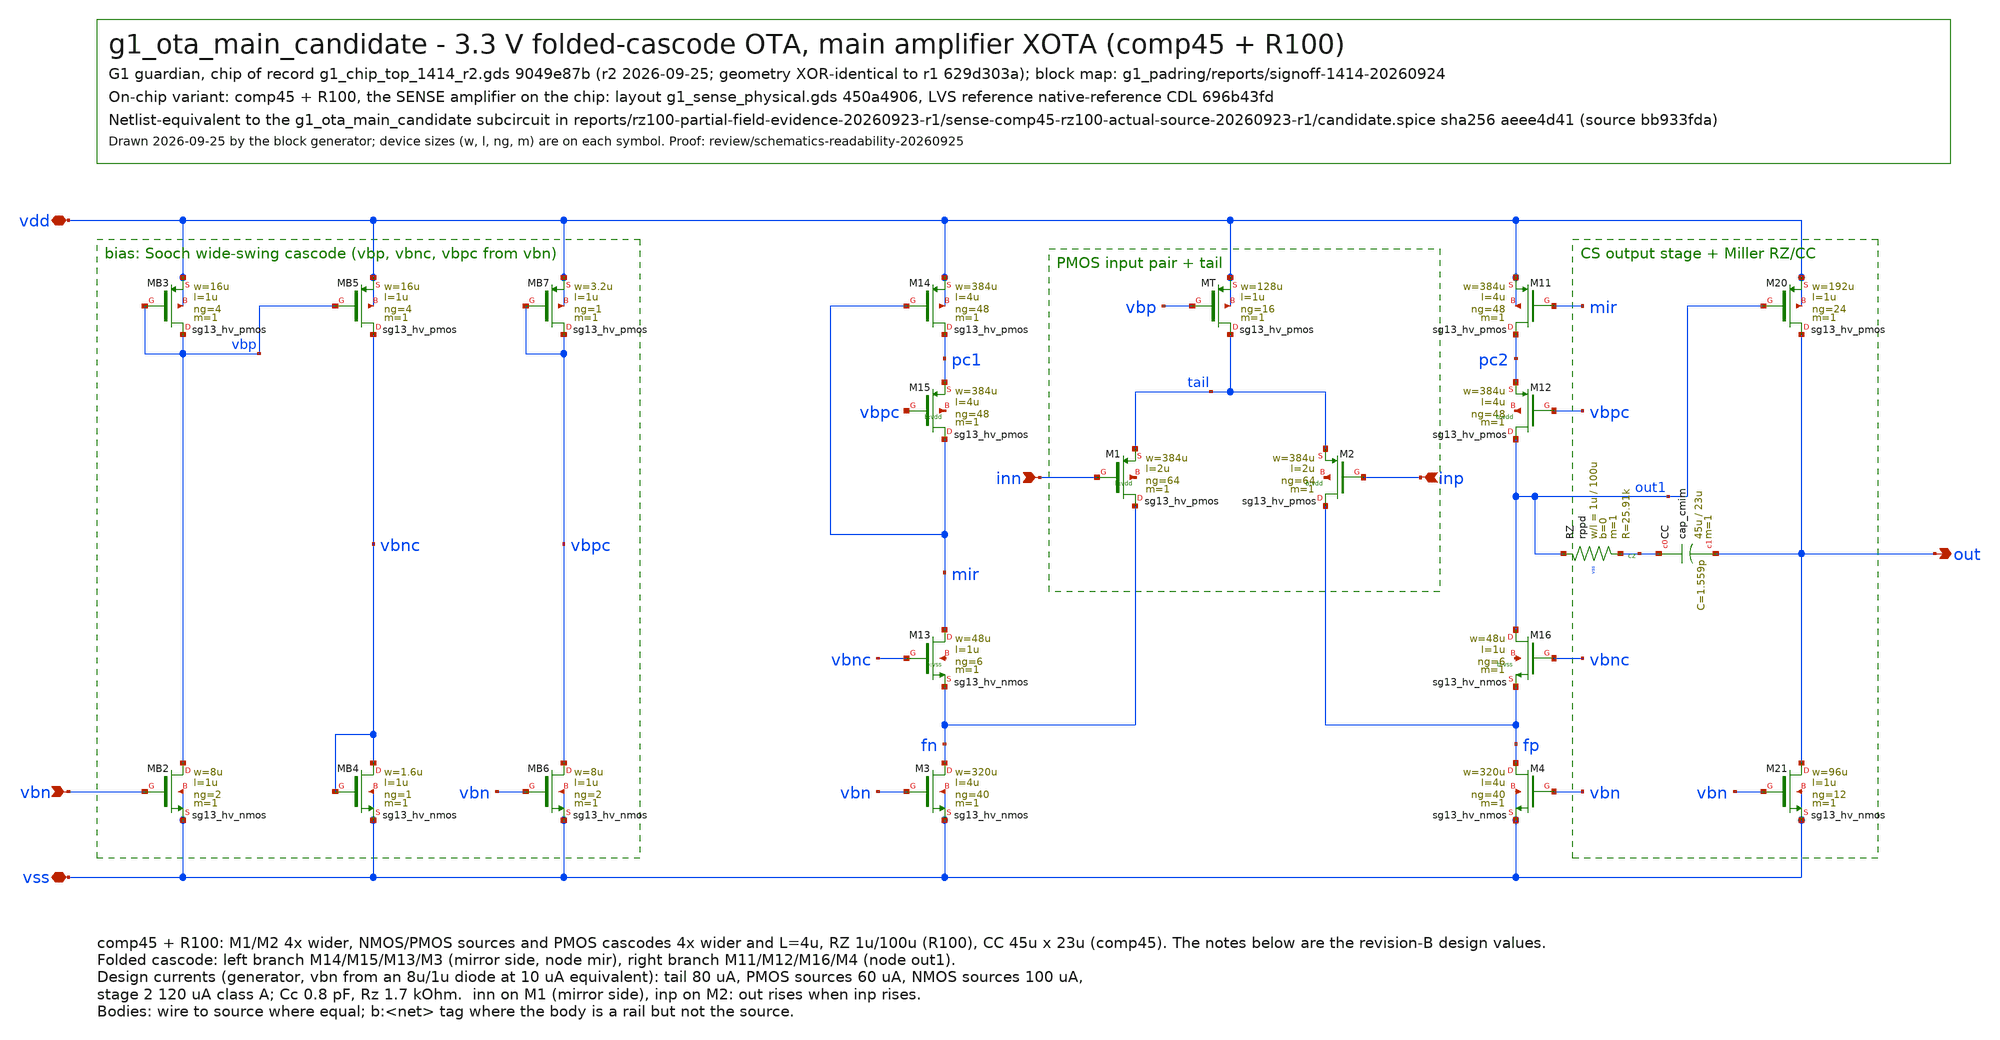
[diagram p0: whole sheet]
** sch_path: designs/g1-guardian/blocks/g1_sense/xschem/comp45_r100/g1_ota_main_candidate.sch
**.subckt g1_ota_main_candidate inp inn vbn out vdd vss
*.ipin inp
*.ipin inn
*.ipin vbn
*.opin out
*.iopin vdd
*.iopin vss
XMB2 vbp vbn vss vss sg13_hv_nmos w=8u l=1u ng=2 m=1 mm_ok=1
XMB3 vbp vbp vdd vdd sg13_hv_pmos w=16u l=1u ng=4 m=1 mm_ok=1
XMB5 vbnc vbp vdd vdd sg13_hv_pmos w=16u l=1u ng=4 m=1 mm_ok=1
XMB4 vbnc vbnc vss vss sg13_hv_nmos w=1.6u l=1u ng=1 m=1 mm_ok=1
XMB6 vbpc vbn vss vss sg13_hv_nmos w=8u l=1u ng=2 m=1 mm_ok=1
XMB7 vbpc vbpc vdd vdd sg13_hv_pmos w=3.2u l=1u ng=1 m=1 mm_ok=1
XMT tail vbp vdd vdd sg13_hv_pmos w=128u l=1u ng=16 m=1 mm_ok=1
XM1 fn inn tail vdd sg13_hv_pmos w=384u l=2u ng=64 m=1 mm_ok=1
XM2 fp inp tail vdd sg13_hv_pmos w=384u l=2u ng=64 m=1 mm_ok=1
XM3 fn vbn vss vss sg13_hv_nmos w=320u l=4u ng=40 m=1 mm_ok=1
XM4 fp vbn vss vss sg13_hv_nmos w=320u l=4u ng=40 m=1 mm_ok=1
XM13 mir vbnc fn vss sg13_hv_nmos w=48u l=1u ng=6 m=1 mm_ok=1
XM16 out1 vbnc fp vss sg13_hv_nmos w=48u l=1u ng=6 m=1 mm_ok=1
XM14 pc1 mir vdd vdd sg13_hv_pmos w=384u l=4u ng=48 m=1 mm_ok=1
XM11 pc2 mir vdd vdd sg13_hv_pmos w=384u l=4u ng=48 m=1 mm_ok=1
XM15 mir vbpc pc1 vdd sg13_hv_pmos w=384u l=4u ng=48 m=1 mm_ok=1
XM12 out1 vbpc pc2 vdd sg13_hv_pmos w=384u l=4u ng=48 m=1 mm_ok=1
XM20 out out1 vdd vdd sg13_hv_pmos w=192u l=1u ng=24 m=1 mm_ok=1
XM21 out vbn vss vss sg13_hv_nmos w=96u l=1u ng=12 m=1 mm_ok=1
XRZ out1 cz vss rppd w=1u l=100u m=1 b=0 mm_ok=1
XCC cz out cap_cmim w=45u l=23u m=1 mm_ok=1
**.ends
.end
